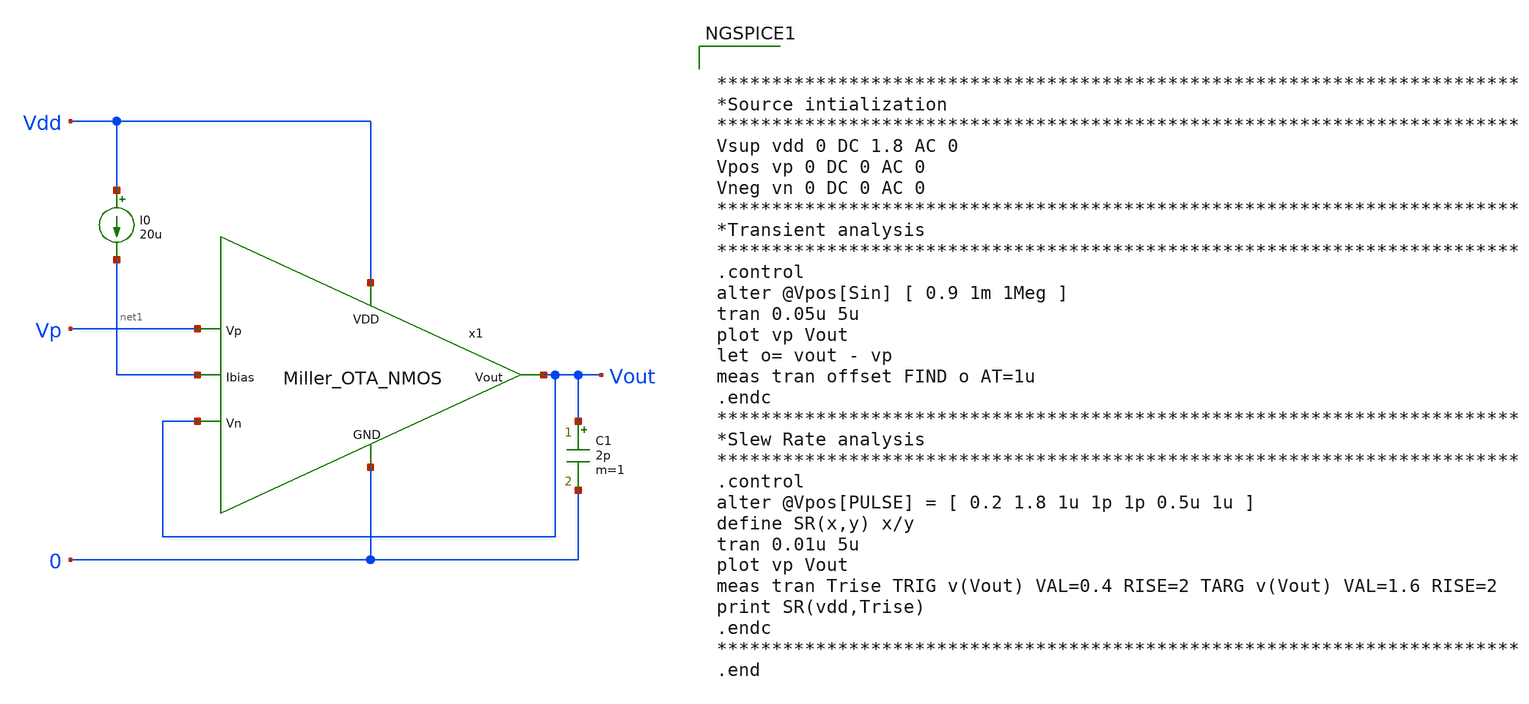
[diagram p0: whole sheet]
** sch_path: Analog_Blocks/OTA/Testbench/Miller_OTA/Transistor5v/Miller_OTA5v_meas_transient.sch
**.subckt Miller_OTA5v_meas_transient
I0 Vdd net1 20u
C1 Vout 0 2p m=1
x1 Vdd Vout Vp Vout net1 0 Miller_OTA_NMOS
**** begin user architecture code

.include ~/Analog_blocks/models/skywater-pdk/libraries/sky130_fd_pr/latest/cells/nfet_01v8/sky130_fd_pr__nfet_01v8__tt.corner.spice
.include ~/Analog_blocks/models/skywater-pdk/libraries/sky130_fd_pr/latest/cells/nfet_01v8_lvt/sky130_fd_pr__nfet_01v8_lvt__tt.corner.spice
.include ~/Analog_blocks/models/skywater-pdk/libraries/sky130_fd_pr/latest/cells/pfet_01v8/sky130_fd_pr__pfet_01v8__tt.corner.spice
.include ~/Analog_blocks/models/skywater-pdk/libraries/sky130_fd_pr/latest/cells/nfet_03v3_nvt/sky130_fd_pr__nfet_03v3_nvt__tt.corner.spice
.include ~/Analog_blocks/models/skywater-pdk/libraries/sky130_fd_pr/latest/cells/nfet_05v0_nvt/sky130_fd_pr__nfet_05v0_nvt__tt.corner.spice
.include ~/Analog_blocks/models/skywater-pdk/libraries/sky130_fd_pr/latest/cells/esd_nfet_01v8/sky130_fd_pr__esd_nfet_01v8__tt.corner.spice
.include ~/Analog_blocks/models/skywater-pdk/libraries/sky130_fd_pr/latest/cells/pfet_01v8_lvt/sky130_fd_pr__pfet_01v8_lvt__tt.corner.spice
.include ~/Analog_blocks/models/skywater-pdk/libraries/sky130_fd_pr/latest/cells/pfet_01v8_hvt/sky130_fd_pr__pfet_01v8_hvt__tt.corner.spice
.include ~/Analog_blocks/models/skywater-pdk/libraries/sky130_fd_pr/latest/cells/esd_pfet_g5v0d10v5/sky130_fd_pr__esd_pfet_g5v0d10v5__tt.corner.spice
.include ~/Analog_blocks/models/skywater-pdk/libraries/sky130_fd_pr/latest/cells/pfet_g5v0d10v5/sky130_fd_pr__pfet_g5v0d10v5__tt.corner.spice
.include ~/Analog_blocks/models/skywater-pdk/libraries/sky130_fd_pr/latest/cells/pfet_g5v0d16v0/sky130_fd_pr__pfet_g5v0d16v0__tt.corner.spice
.include ~/Analog_blocks/models/skywater-pdk/libraries/sky130_fd_pr/latest/cells/nfet_g5v0d10v5/sky130_fd_pr__nfet_g5v0d10v5__tt.corner.spice
.include ~/Analog_blocks/models/skywater-pdk/libraries/sky130_fd_pr/latest/cells/nfet_g5v0d16v0/sky130_fd_pr__nfet_g5v0d16v0__tt_discrete.corner.spice
.include ~/Analog_blocks/models/skywater-pdk/libraries/sky130_fd_pr/latest/cells/esd_nfet_g5v0d10v5/sky130_fd_pr__esd_nfet_g5v0d10v5__tt.corner.spice
.include ~/Analog_blocks/models/skywater-pdk/libraries/sky130_fd_pr/latest/models/corners/tt/nonfet.spice
* Mismatch parameters
.include ~/Analog_blocks/models/skywater-pdk/libraries/sky130_fd_pr/latest/cells/nfet_01v8/sky130_fd_pr__nfet_01v8__mismatch.corner.spice
.include ~/Analog_blocks/models/skywater-pdk/libraries/sky130_fd_pr/latest/cells/pfet_01v8/sky130_fd_pr__pfet_01v8__mismatch.corner.spice
.include ~/Analog_blocks/models/skywater-pdk/libraries/sky130_fd_pr/latest/cells/nfet_01v8_lvt/sky130_fd_pr__nfet_01v8_lvt__mismatch.corner.spice
.include ~/Analog_blocks/models/skywater-pdk/libraries/sky130_fd_pr/latest/cells/pfet_01v8_lvt/sky130_fd_pr__pfet_01v8_lvt__mismatch.corner.spice
.include ~/Analog_blocks/models/skywater-pdk/libraries/sky130_fd_pr/latest/cells/pfet_01v8_hvt/sky130_fd_pr__pfet_01v8_hvt__mismatch.corner.spice
.include ~/Analog_blocks/models/skywater-pdk/libraries/sky130_fd_pr/latest/cells/nfet_g5v0d10v5/sky130_fd_pr__nfet_g5v0d10v5__mismatch.corner.spice
.include ~/Analog_blocks/models/skywater-pdk/libraries/sky130_fd_pr/latest/cells/pfet_g5v0d10v5/sky130_fd_pr__pfet_g5v0d10v5__mismatch.corner.spice
.include ~/Analog_blocks/models/skywater-pdk/libraries/sky130_fd_pr/latest/cells/nfet_05v0_nvt/sky130_fd_pr__nfet_05v0_nvt__mismatch.corner.spice
.include ~/Analog_blocks/models/skywater-pdk/libraries/sky130_fd_pr/latest/cells/nfet_03v3_nvt/sky130_fd_pr__nfet_03v3_nvt__mismatch.corner.spice
* Resistor
.include ~/Analog_blocks/models/skywater-pdk/libraries/sky130_fd_pr/latest/models/r+c/res_typical__cap_typical.spice
.include ~/Analog_blocks/models/skywater-pdk/libraries/sky130_fd_pr/latest/models/r+c/res_typical__cap_typical__lin.spice
* Special cells
.include ~/Analog_blocks/models/skywater-pdk/libraries/sky130_fd_pr/latest/models/corners/tt/specialized_cells.spice
* All models
.include ~/Analog_blocks/models/skywater-pdk/libraries/sky130_fd_pr/latest/models/all.spice
* Corner
.include ~/Analog_blocks/models/skywater-pdk/libraries/sky130_fd_pr/latest/models/corners/tt/rf.spice



*************************************************************************
*Source intialization
*************************************************************************
Vsup vdd 0 DC 1.8 AC 0
Vpos vp 0 DC 0 AC 0
Vneg vn 0 DC 0 AC 0
*************************************************************************
*Transient analysis
*************************************************************************
.control
alter @Vpos[Sin] [ 0.9 1m 1Meg ]
tran 0.05u 5u
plot vp Vout
let o= vout - vp
meas tran offset FIND o AT=1u
.endc
*************************************************************************
*Slew Rate analysis
*************************************************************************
.control
alter @Vpos[PULSE] = [ 0.2 1.8 1u 1p 1p 0.5u 1u ]
define SR(x,y) x/y
tran 0.01u 5u
plot vp Vout
meas tran Trise TRIG v(Vout) VAL=0.4 RISE=2 TARG v(Vout) VAL=1.6 RISE=2
print SR(vdd,Trise)
.endc
*************************************************************************
.end


**** end user architecture code
**.ends

* expanding   symbol:
*+  /home/eslam/Analog_blocks/Analog_Blocks/OTA/Schematic/Miller_OTA/Transistor5v/Miller_OTA_NMOS.sym # of pins=6
** sym_path: Analog_Blocks/OTA/Schematic/Miller_OTA/Transistor5v/Miller_OTA_NMOS.sym
** sch_path: Analog_Blocks/OTA/Schematic/Miller_OTA/Transistor5v/Miller_OTA_NMOS.sch
.subckt Miller_OTA_NMOS VDD Vn Vp Vout Ibias GND
*.ipin VDD
*.ipin Ibias
*.ipin Vn
*.ipin Vp
*.opin Vout
*.ipin GND
XM1 net1 Vn net3 GND sky130_fd_pr__nfet_g5v0d10v5 L=0.5 W=10 nf=1 ad='int((nf+1)/2) * W/nf * 0.29' as='int((nf+2)/2) * W/nf * 0.29'
+ pd='2*int((nf+1)/2) * (W/nf + 0.29)' ps='2*int((nf+2)/2) * (W/nf + 0.29)' nrd='0.29 / W' nrs='0.29 / W'
+ sa=0 sb=0 sd=0 mult=8 m=8
XM2 net2 Vp net3 GND sky130_fd_pr__nfet_g5v0d10v5 L=0.5 W=10 nf=1 ad='int((nf+1)/2) * W/nf * 0.29' as='int((nf+2)/2) * W/nf * 0.29'
+ pd='2*int((nf+1)/2) * (W/nf + 0.29)' ps='2*int((nf+2)/2) * (W/nf + 0.29)' nrd='0.29 / W' nrs='0.29 / W'
+ sa=0 sb=0 sd=0 mult=8 m=8
XM3 net1 net1 VDD VDD sky130_fd_pr__pfet_g5v0d10v5 L=0.5 W=5 nf=1 ad='int((nf+1)/2) * W/nf * 0.29' as='int((nf+2)/2) * W/nf * 0.29'
+ pd='2*int((nf+1)/2) * (W/nf + 0.29)' ps='2*int((nf+2)/2) * (W/nf + 0.29)' nrd='0.29 / W' nrs='0.29 / W'
+ sa=0 sb=0 sd=0 mult=4 m=4
XM4 net2 net1 VDD VDD sky130_fd_pr__pfet_g5v0d10v5 L=0.5 W=5 nf=1 ad='int((nf+1)/2) * W/nf * 0.29' as='int((nf+2)/2) * W/nf * 0.29'
+ pd='2*int((nf+1)/2) * (W/nf + 0.29)' ps='2*int((nf+2)/2) * (W/nf + 0.29)' nrd='0.29 / W' nrs='0.29 / W'
+ sa=0 sb=0 sd=0 mult=4 m=4
XM6 Vout net2 VDD VDD sky130_fd_pr__pfet_g5v0d10v5 L=0.5 W=5 nf=1 ad='int((nf+1)/2) * W/nf * 0.29' as='int((nf+2)/2) * W/nf * 0.29'
+ pd='2*int((nf+1)/2) * (W/nf + 0.29)' ps='2*int((nf+2)/2) * (W/nf + 0.29)' nrd='0.29 / W' nrs='0.29 / W'
+ sa=0 sb=0 sd=0 mult=20 m=20
XM5 net3 Ibias GND GND sky130_fd_pr__nfet_g5v0d10v5 L=1 W=3 nf=1 ad='int((nf+1)/2) * W/nf * 0.29' as='int((nf+2)/2) * W/nf * 0.29'
+ pd='2*int((nf+1)/2) * (W/nf + 0.29)' ps='2*int((nf+2)/2) * (W/nf + 0.29)' nrd='0.29 / W' nrs='0.29 / W'
+ sa=0 sb=0 sd=0 mult=8 m=8
XM8 Ibias Ibias GND GND sky130_fd_pr__nfet_g5v0d10v5 L=1 W=3 nf=1 ad='int((nf+1)/2) * W/nf * 0.29' as='int((nf+2)/2) * W/nf * 0.29'
+ pd='2*int((nf+1)/2) * (W/nf + 0.29)' ps='2*int((nf+2)/2) * (W/nf + 0.29)' nrd='0.29 / W' nrs='0.29 / W'
+ sa=0 sb=0 sd=0 mult=8 m=8
XC1 net2 Vout sky130_fd_pr__cap_mim_m3_2 W=25 L=25 MF=1 m=1
XM7 Vout Ibias GND GND sky130_fd_pr__nfet_g5v0d10v5 L=1 W=3 nf=1 ad='int((nf+1)/2) * W/nf * 0.29' as='int((nf+2)/2) * W/nf * 0.29'
+ pd='2*int((nf+1)/2) * (W/nf + 0.29)' ps='2*int((nf+2)/2) * (W/nf + 0.29)' nrd='0.29 / W' nrs='0.29 / W'
+ sa=0 sb=0 sd=0 mult=16 m=16
.ends

.end
